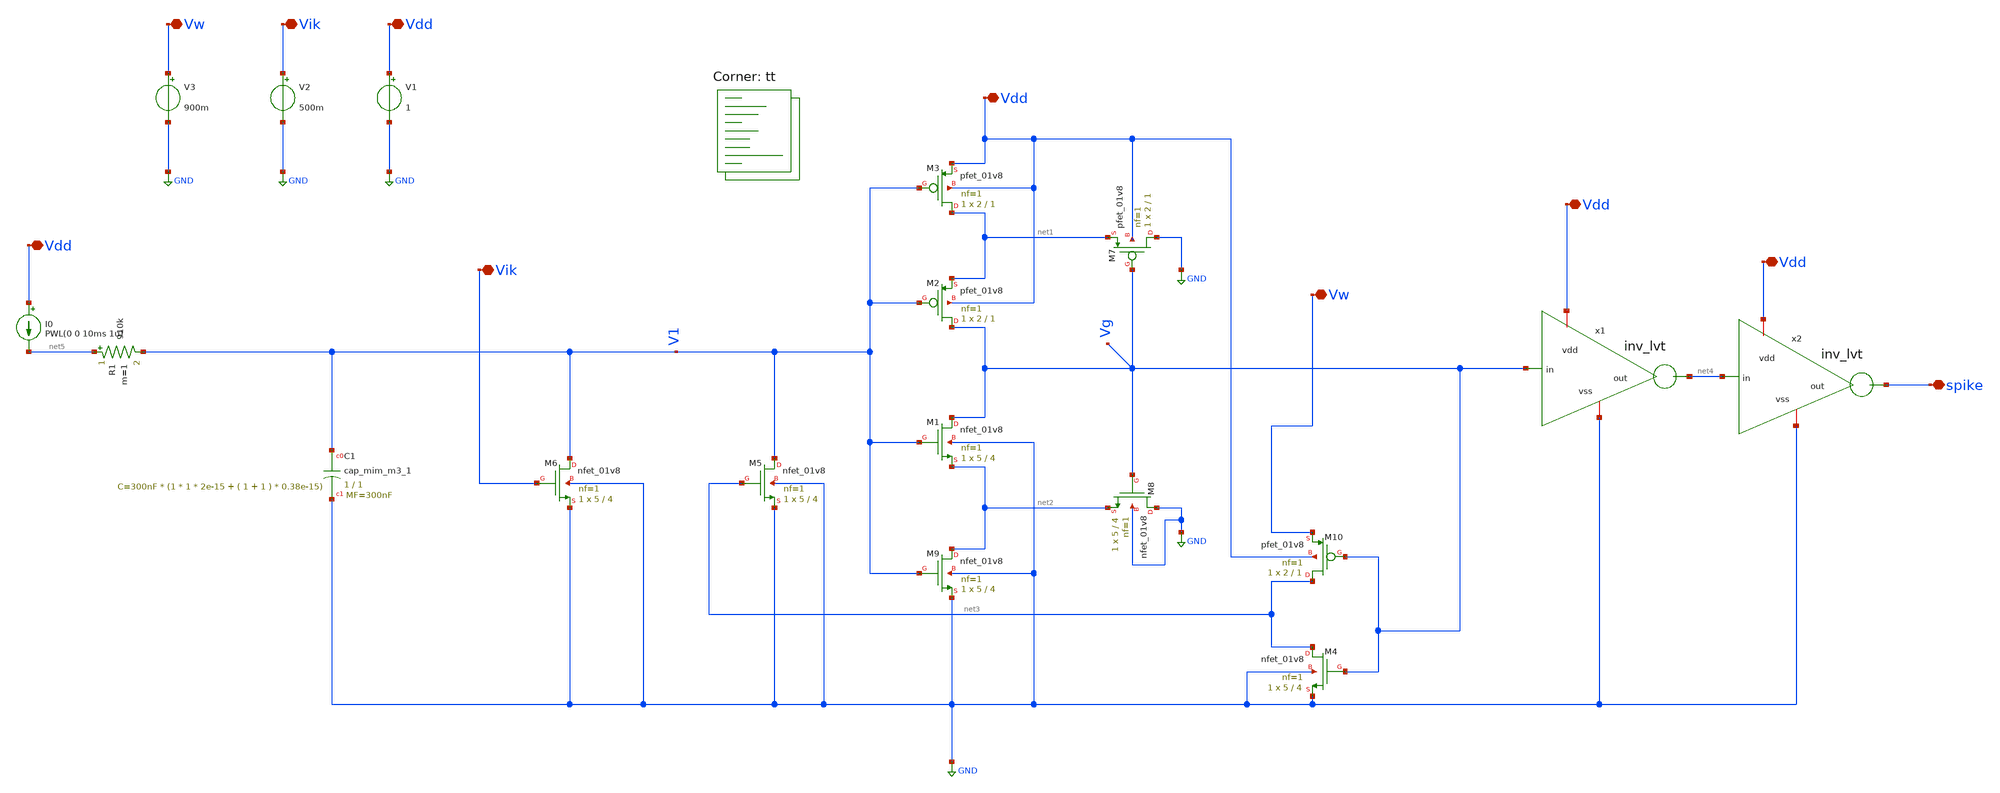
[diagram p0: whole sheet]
** sch_path: DIMAS/LIF.sch
**.subckt LIF Vdd Vw spike Vik Vdd Vdd Vik Vw Vdd Vdd
*.iopin Vdd
*.iopin Vw
*.iopin spike
*.iopin Vik
*.iopin Vdd
*.iopin Vdd
*.iopin Vik
*.iopin Vw
*.iopin Vdd
*.iopin Vdd
XM1 Vg V1 net2 GND sky130_fd_pr__nfet_01v8 L=4 W=5 nf=1 ad='int((nf+1)/2) * W/nf * 0.29' as='int((nf+2)/2) * W/nf * 0.29'
+ pd='2*int((nf+1)/2) * (W/nf + 0.29)' ps='2*int((nf+2)/2) * (W/nf + 0.29)' nrd='0.29 / W' nrs='0.29 / W'
+ sa=0 sb=0 sd=0 mult=1 m=1
XM2 Vg V1 net1 Vdd sky130_fd_pr__pfet_01v8 L=1 W=2 nf=1 ad='int((nf+1)/2) * W/nf * 0.29' as='int((nf+2)/2) * W/nf * 0.29'
+ pd='2*int((nf+1)/2) * (W/nf + 0.29)' ps='2*int((nf+2)/2) * (W/nf + 0.29)' nrd='0.29 / W' nrs='0.29 / W'
+ sa=0 sb=0 sd=0 mult=1 m=1
XC1 V1 GND sky130_fd_pr__cap_mim_m3_1 W=1 L=1 MF=300nF m=300nF
XM3 net1 V1 Vdd Vdd sky130_fd_pr__pfet_01v8 L=1 W=2 nf=1 ad='int((nf+1)/2) * W/nf * 0.29' as='int((nf+2)/2) * W/nf * 0.29'
+ pd='2*int((nf+1)/2) * (W/nf + 0.29)' ps='2*int((nf+2)/2) * (W/nf + 0.29)' nrd='0.29 / W' nrs='0.29 / W'
+ sa=0 sb=0 sd=0 mult=1 m=1
XM4 net3 Vg GND GND sky130_fd_pr__nfet_01v8 L=4 W=5 nf=1 ad='int((nf+1)/2) * W/nf * 0.29' as='int((nf+2)/2) * W/nf * 0.29'
+ pd='2*int((nf+1)/2) * (W/nf + 0.29)' ps='2*int((nf+2)/2) * (W/nf + 0.29)' nrd='0.29 / W' nrs='0.29 / W'
+ sa=0 sb=0 sd=0 mult=1 m=1
XM5 V1 net3 GND GND sky130_fd_pr__nfet_01v8 L=4 W=5 nf=1 ad='int((nf+1)/2) * W/nf * 0.29' as='int((nf+2)/2) * W/nf * 0.29'
+ pd='2*int((nf+1)/2) * (W/nf + 0.29)' ps='2*int((nf+2)/2) * (W/nf + 0.29)' nrd='0.29 / W' nrs='0.29 / W'
+ sa=0 sb=0 sd=0 mult=1 m=1
XM6 V1 Vik GND GND sky130_fd_pr__nfet_01v8 L=4 W=5 nf=1 ad='int((nf+1)/2) * W/nf * 0.29' as='int((nf+2)/2) * W/nf * 0.29'
+ pd='2*int((nf+1)/2) * (W/nf + 0.29)' ps='2*int((nf+2)/2) * (W/nf + 0.29)' nrd='0.29 / W' nrs='0.29 / W'
+ sa=0 sb=0 sd=0 mult=1 m=1
XM7 GND Vg net1 Vdd sky130_fd_pr__pfet_01v8 L=1 W=2 nf=1 ad='int((nf+1)/2) * W/nf * 0.29' as='int((nf+2)/2) * W/nf * 0.29'
+ pd='2*int((nf+1)/2) * (W/nf + 0.29)' ps='2*int((nf+2)/2) * (W/nf + 0.29)' nrd='0.29 / W' nrs='0.29 / W'
+ sa=0 sb=0 sd=0 mult=1 m=1
XM8 GND Vg net2 GND sky130_fd_pr__nfet_01v8 L=4 W=5 nf=1 ad='int((nf+1)/2) * W/nf * 0.29' as='int((nf+2)/2) * W/nf * 0.29'
+ pd='2*int((nf+1)/2) * (W/nf + 0.29)' ps='2*int((nf+2)/2) * (W/nf + 0.29)' nrd='0.29 / W' nrs='0.29 / W'
+ sa=0 sb=0 sd=0 mult=1 m=1
XM9 net2 V1 GND GND sky130_fd_pr__nfet_01v8 L=4 W=5 nf=1 ad='int((nf+1)/2) * W/nf * 0.29' as='int((nf+2)/2) * W/nf * 0.29'
+ pd='2*int((nf+1)/2) * (W/nf + 0.29)' ps='2*int((nf+2)/2) * (W/nf + 0.29)' nrd='0.29 / W' nrs='0.29 / W'
+ sa=0 sb=0 sd=0 mult=1 m=1
XM10 net3 Vg Vw Vdd sky130_fd_pr__pfet_01v8 L=1 W=2 nf=1 ad='int((nf+1)/2) * W/nf * 0.29' as='int((nf+2)/2) * W/nf * 0.29'
+ pd='2*int((nf+1)/2) * (W/nf + 0.29)' ps='2*int((nf+2)/2) * (W/nf + 0.29)' nrd='0.29 / W' nrs='0.29 / W'
+ sa=0 sb=0 sd=0 mult=1 m=1
x1 Vdd Vg net4 GND inv_lvt
V1 Vdd GND 1
I0 Vdd net5 PWL(0 0 10ms 1u)
V2 Vik GND 500m
V3 Vw GND 900m
R1 net5 V1 910k m=1
x2 Vdd net4 spike GND inv_lvt
**** begin user architecture code
.lib $::SKYWATER_MODELS/sky130.lib.spice tt
**** end user architecture code
**.ends

* expanding   symbol:  inv_lvt.sym # of pins=4
** sym_path: DIMAS/inv_lvt.sym
** sch_path: DIMAS/inv_lvt.sch
.subckt inv_lvt vdd in out vss
*.iopin vdd
*.iopin vss
*.ipin in
*.opin out
XM1 out in vdd vdd sky130_fd_pr__pfet_01v8_lvt L=0.4 W=1 nf=1 ad='int((nf+1)/2) * W/nf * 0.29' as='int((nf+2)/2) * W/nf * 0.29'
+ pd='2*int((nf+1)/2) * (W/nf + 0.29)' ps='2*int((nf+2)/2) * (W/nf + 0.29)' nrd='0.29 / W' nrs='0.29 / W'
+ sa=0 sb=0 sd=0 mult=1 m=1
XM2 out in vss vss sky130_fd_pr__nfet_01v8_lvt L=0.4 W=1 nf=1 ad='int((nf+1)/2) * W/nf * 0.29' as='int((nf+2)/2) * W/nf * 0.29'
+ pd='2*int((nf+1)/2) * (W/nf + 0.29)' ps='2*int((nf+2)/2) * (W/nf + 0.29)' nrd='0.29 / W' nrs='0.29 / W'
+ sa=0 sb=0 sd=0 mult=1 m=1
.ends

.GLOBAL GND
**** begin user architecture code

.options savecurrents
.tran 100n 10m uic
.save all
.control
	run
	set wr_vecnames
	set wr_singlescale
	wrdata datos.txt @i0[current] spike
.endc


**** end user architecture code
.end
